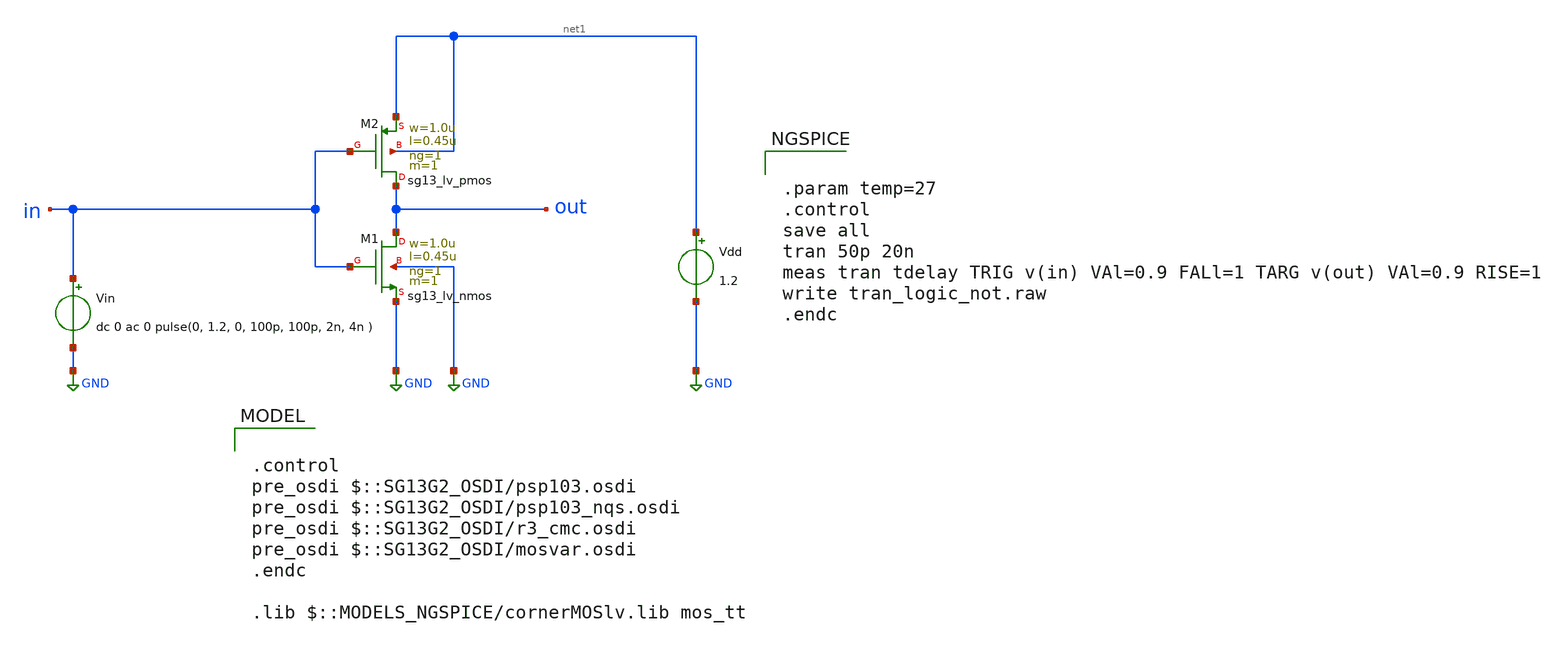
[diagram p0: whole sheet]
** sch_path: ihp-sg13g2/xschem_libs/sg13g2_tests/tran_logic_not/schematic/tran_logic_not.sch
* Copyright 2023 IHP PDK Authors
**.subckt tran_logic_not
Vin in GND dc 0 ac 0 pulse(0, 1.2, 0, 100p, 100p, 2n, 4n )
Vdd net1 GND 1.2
XM1 out in GND GND sg13_lv_nmos w=1.0u l=0.45u ng=1 m=1 mm_ok=1
XM2 out in net1 net1 sg13_lv_pmos w=1.0u l=0.45u ng=1 m=1 mm_ok=1
**** begin user architecture code

.control
pre_osdi $::SG13G2_OSDI/psp103.osdi
pre_osdi $::SG13G2_OSDI/psp103_nqs.osdi
pre_osdi $::SG13G2_OSDI/r3_cmc.osdi
pre_osdi $::SG13G2_OSDI/mosvar.osdi
.endc

.lib $::MODELS_NGSPICE/cornerMOSlv.lib mos_tt



.param temp=27
.control
save all
tran 50p 20n
meas tran tdelay TRIG v(in) VAl=0.9 FALl=1 TARG v(out) VAl=0.9 RISE=1
write tran_logic_not.raw
.endc


**** end user architecture code
**.ends
.GLOBAL GND
.end
